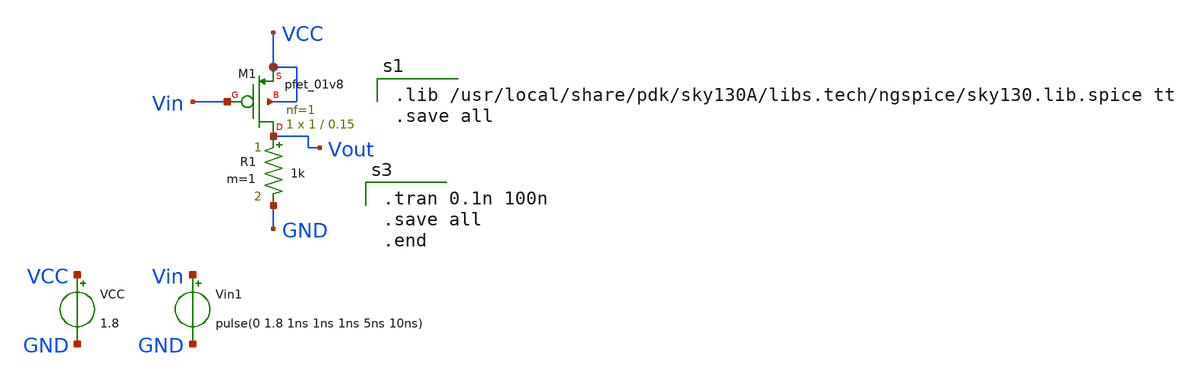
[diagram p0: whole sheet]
** sch_path: Schematic/pmos.sch
**.subckt pmos
VCC VCC GND 1.8
Vin1 Vin GND pulse(0 1.8 1ns 1ns 1ns 5ns 10ns)
XM1 Vout Vin VCC VCC sky130_fd_pr__pfet_01v8 L=0.15 W=1 nf=1 ad='int((nf+1)/2) * W/nf * 0.29' as='int((nf+2)/2) * W/nf * 0.29'
+ pd='2*int((nf+1)/2) * (W/nf + 0.29)' ps='2*int((nf+2)/2) * (W/nf + 0.29)' nrd='0.29 / W' nrs='0.29 / W'
+ sa=0 sb=0 sd=0 mult=1 m=1
R1 Vout GND 1k m=1
**** begin user architecture code

.lib /usr/local/share/pdk/sky130A/libs.tech/ngspice/sky130.lib.spice tt
.save all


.tran 0.1n 100n
.save all
.end

**** end user architecture code
**.ends
.end
